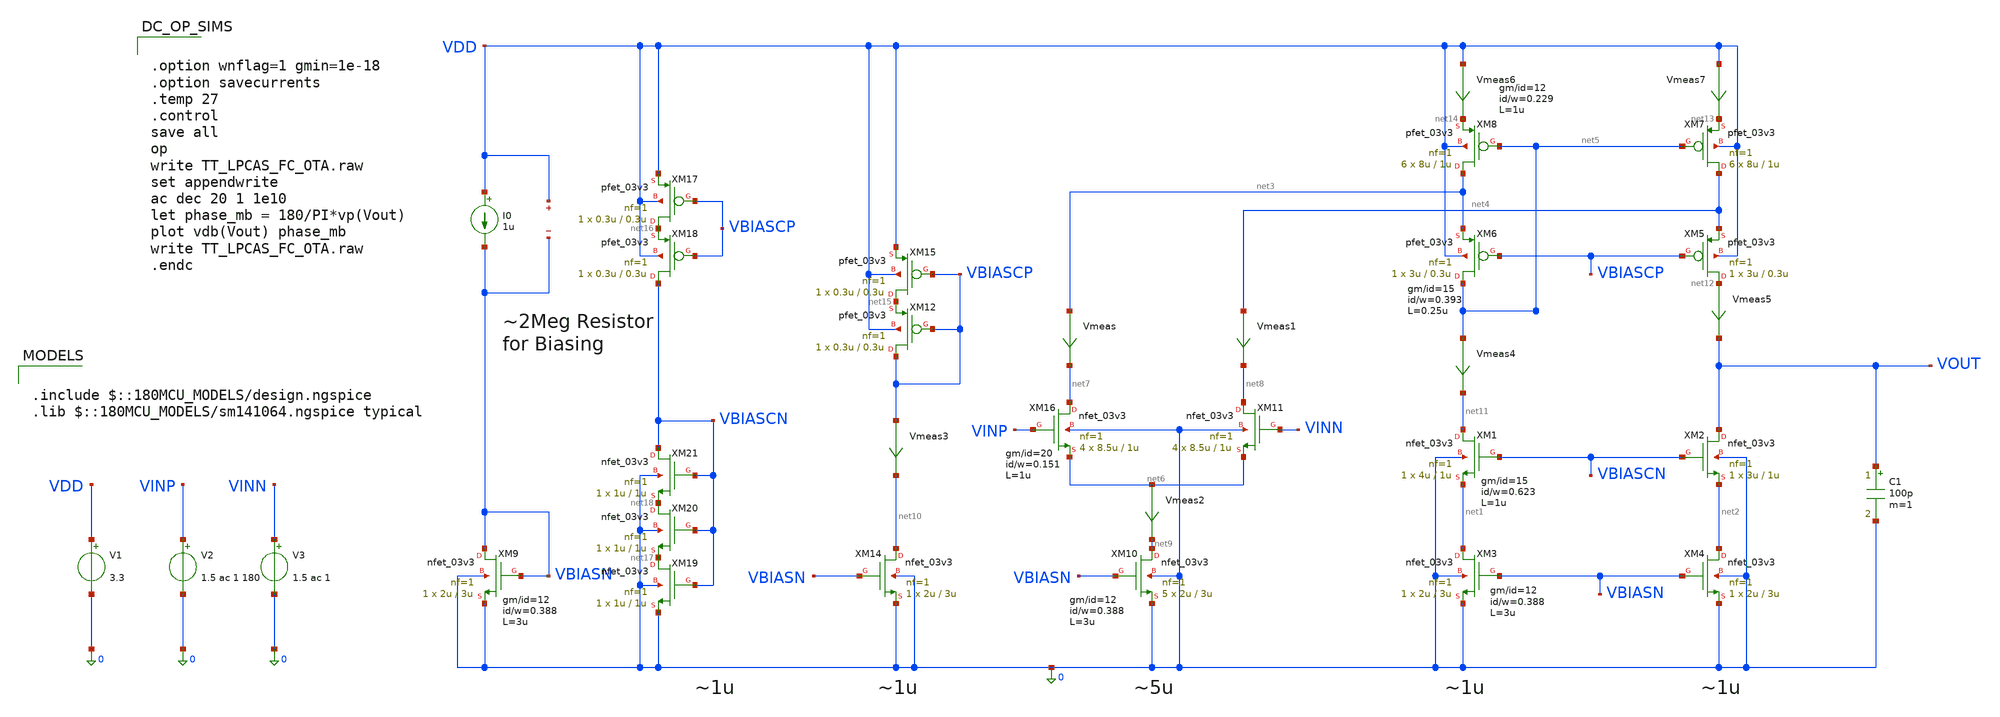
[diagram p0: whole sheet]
** sch_path: SCH/TT_LPCAS_FC_OTA.sch
**.subckt TT_LPCAS_FC_OTA
XM1 net11 VBIASCN net1 0 nfet_03v3 L=1u W=4u nf=1 ad='int((nf+1)/2) * W/nf * 0.18u' as='int((nf+2)/2) * W/nf * 0.18u'
+ pd='2*int((nf+1)/2) * (W/nf + 0.18u)' ps='2*int((nf+2)/2) * (W/nf + 0.18u)' nrd='0.18u / W' nrs='0.18u / W'
+ sa=0 sb=0 sd=0 m=1
XM2 VOUT VBIASCN net2 0 nfet_03v3 L=1u W=3u nf=1 ad='int((nf+1)/2) * W/nf * 0.18u' as='int((nf+2)/2) * W/nf * 0.18u'
+ pd='2*int((nf+1)/2) * (W/nf + 0.18u)' ps='2*int((nf+2)/2) * (W/nf + 0.18u)' nrd='0.18u / W' nrs='0.18u / W'
+ sa=0 sb=0 sd=0 m=1
XM5 net12 VBIASCP net4 VDD pfet_03v3 L=0.3u W=3u nf=1 ad='int((nf+1)/2) * W/nf * 0.18u' as='int((nf+2)/2) * W/nf * 0.18u'
+ pd='2*int((nf+1)/2) * (W/nf + 0.18u)' ps='2*int((nf+2)/2) * (W/nf + 0.18u)' nrd='0.18u / W' nrs='0.18u / W'
+ sa=0 sb=0 sd=0 m=1
XM6 net5 VBIASCP net3 VDD pfet_03v3 L=0.3u W=3u nf=1 ad='int((nf+1)/2) * W/nf * 0.18u' as='int((nf+2)/2) * W/nf * 0.18u'
+ pd='2*int((nf+1)/2) * (W/nf + 0.18u)' ps='2*int((nf+2)/2) * (W/nf + 0.18u)' nrd='0.18u / W' nrs='0.18u / W'
+ sa=0 sb=0 sd=0 m=1
XM7 net4 net5 net13 VDD pfet_03v3 L=1u W=8u nf=1 ad='int((nf+1)/2) * W/nf * 0.18u' as='int((nf+2)/2) * W/nf * 0.18u'
+ pd='2*int((nf+1)/2) * (W/nf + 0.18u)' ps='2*int((nf+2)/2) * (W/nf + 0.18u)' nrd='0.18u / W' nrs='0.18u / W'
+ sa=0 sb=0 sd=0 m=6
XM8 net3 net5 net14 VDD pfet_03v3 L=1u W=8u nf=1 ad='int((nf+1)/2) * W/nf * 0.18u' as='int((nf+2)/2) * W/nf * 0.18u'
+ pd='2*int((nf+1)/2) * (W/nf + 0.18u)' ps='2*int((nf+2)/2) * (W/nf + 0.18u)' nrd='0.18u / W' nrs='0.18u / W'
+ sa=0 sb=0 sd=0 m=6
XM9 VBIASN VBIASN 0 0 nfet_03v3 L=3u W=2u nf=1 ad='int((nf+1)/2) * W/nf * 0.18u' as='int((nf+2)/2) * W/nf * 0.18u'
+ pd='2*int((nf+1)/2) * (W/nf + 0.18u)' ps='2*int((nf+2)/2) * (W/nf + 0.18u)' nrd='0.18u / W' nrs='0.18u / W'
+ sa=0 sb=0 sd=0 m=1
XM10 net9 VBIASN 0 0 nfet_03v3 L=3u W=2u nf=1 ad='int((nf+1)/2) * W/nf * 0.18u' as='int((nf+2)/2) * W/nf * 0.18u'
+ pd='2*int((nf+1)/2) * (W/nf + 0.18u)' ps='2*int((nf+2)/2) * (W/nf + 0.18u)' nrd='0.18u / W' nrs='0.18u / W'
+ sa=0 sb=0 sd=0 m=5
XM3 net1 VBIASN 0 0 nfet_03v3 L=3u W=2u nf=1 ad='int((nf+1)/2) * W/nf * 0.18u' as='int((nf+2)/2) * W/nf * 0.18u'
+ pd='2*int((nf+1)/2) * (W/nf + 0.18u)' ps='2*int((nf+2)/2) * (W/nf + 0.18u)' nrd='0.18u / W' nrs='0.18u / W'
+ sa=0 sb=0 sd=0 m=1
XM4 net2 VBIASN 0 0 nfet_03v3 L=3u W=2u nf=1 ad='int((nf+1)/2) * W/nf * 0.18u' as='int((nf+2)/2) * W/nf * 0.18u'
+ pd='2*int((nf+1)/2) * (W/nf + 0.18u)' ps='2*int((nf+2)/2) * (W/nf + 0.18u)' nrd='0.18u / W' nrs='0.18u / W'
+ sa=0 sb=0 sd=0 m=1
XM14 net10 VBIASN 0 0 nfet_03v3 L=3u W=2u nf=1 ad='int((nf+1)/2) * W/nf * 0.18u' as='int((nf+2)/2) * W/nf * 0.18u'
+ pd='2*int((nf+1)/2) * (W/nf + 0.18u)' ps='2*int((nf+2)/2) * (W/nf + 0.18u)' nrd='0.18u / W' nrs='0.18u / W'
+ sa=0 sb=0 sd=0 m=1
XM15 net15 VBIASCP VDD VDD pfet_03v3 L=0.3u W=0.3u nf=1 ad='int((nf+1)/2) * W/nf * 0.18u' as='int((nf+2)/2) * W/nf * 0.18u'
+ pd='2*int((nf+1)/2) * (W/nf + 0.18u)' ps='2*int((nf+2)/2) * (W/nf + 0.18u)' nrd='0.18u / W' nrs='0.18u / W'
+ sa=0 sb=0 sd=0 m=1
I0 VDD VBIASN 1u
Vmeas net3 net7 0
.save i(vmeas)
Vmeas1 net4 net8 0
.save i(vmeas1)
Vmeas2 net6 net9 0
.save i(vmeas2)
Vmeas3 VBIASCP net10 0
.save i(vmeas3)
Vmeas4 net5 net11 0
.save i(vmeas4)
Vmeas5 net12 VOUT 0
.save i(vmeas5)
XM16 net7 VINP net6 0 nfet_03v3 L=1u W=8.5u nf=1 ad='int((nf+1)/2) * W/nf * 0.18u' as='int((nf+2)/2) * W/nf * 0.18u'
+ pd='2*int((nf+1)/2) * (W/nf + 0.18u)' ps='2*int((nf+2)/2) * (W/nf + 0.18u)' nrd='0.18u / W' nrs='0.18u / W'
+ sa=0 sb=0 sd=0 m=4
XM11 net8 VINN net6 0 nfet_03v3 L=1u W=8.5u nf=1 ad='int((nf+1)/2) * W/nf * 0.18u' as='int((nf+2)/2) * W/nf * 0.18u'
+ pd='2*int((nf+1)/2) * (W/nf + 0.18u)' ps='2*int((nf+2)/2) * (W/nf + 0.18u)' nrd='0.18u / W' nrs='0.18u / W'
+ sa=0 sb=0 sd=0 m=4
V1 VDD 0 3.3
V2 VINP 0 1.5 ac 1 180
V3 VINN 0 1.5 ac 1
Vmeas6 VDD net14 0
.save i(vmeas6)
Vmeas7 VDD net13 0
.save i(vmeas7)
C1 VOUT 0 100p m=1
XM12 VBIASCP VBIASCP net15 VDD pfet_03v3 L=0.3u W=0.3u nf=1 ad='int((nf+1)/2) * W/nf * 0.18u' as='int((nf+2)/2) * W/nf * 0.18u'
+ pd='2*int((nf+1)/2) * (W/nf + 0.18u)' ps='2*int((nf+2)/2) * (W/nf + 0.18u)' nrd='0.18u / W' nrs='0.18u / W'
+ sa=0 sb=0 sd=0 m=1
XM17 net16 VBIASCP VDD VDD pfet_03v3 L=0.3u W=0.3u nf=1 ad='int((nf+1)/2) * W/nf * 0.18u' as='int((nf+2)/2) * W/nf * 0.18u'
+ pd='2*int((nf+1)/2) * (W/nf + 0.18u)' ps='2*int((nf+2)/2) * (W/nf + 0.18u)' nrd='0.18u / W' nrs='0.18u / W'
+ sa=0 sb=0 sd=0 m=1
XM18 VBIASCN VBIASCP net16 VDD pfet_03v3 L=0.3u W=0.3u nf=1 ad='int((nf+1)/2) * W/nf * 0.18u' as='int((nf+2)/2) * W/nf * 0.18u'
+ pd='2*int((nf+1)/2) * (W/nf + 0.18u)' ps='2*int((nf+2)/2) * (W/nf + 0.18u)' nrd='0.18u / W' nrs='0.18u / W'
+ sa=0 sb=0 sd=0 m=1
XM19 net17 VBIASCN 0 0 nfet_03v3 L=1u W=1u nf=1 ad='int((nf+1)/2) * W/nf * 0.18u' as='int((nf+2)/2) * W/nf * 0.18u'
+ pd='2*int((nf+1)/2) * (W/nf + 0.18u)' ps='2*int((nf+2)/2) * (W/nf + 0.18u)' nrd='0.18u / W' nrs='0.18u / W'
+ sa=0 sb=0 sd=0 m=1
XM20 net18 VBIASCN net17 0 nfet_03v3 L=1u W=1u nf=1 ad='int((nf+1)/2) * W/nf * 0.18u' as='int((nf+2)/2) * W/nf * 0.18u'
+ pd='2*int((nf+1)/2) * (W/nf + 0.18u)' ps='2*int((nf+2)/2) * (W/nf + 0.18u)' nrd='0.18u / W' nrs='0.18u / W'
+ sa=0 sb=0 sd=0 m=1
XM21 VBIASCN VBIASCN net18 0 nfet_03v3 L=1u W=1u nf=1 ad='int((nf+1)/2) * W/nf * 0.18u' as='int((nf+2)/2) * W/nf * 0.18u'
+ pd='2*int((nf+1)/2) * (W/nf + 0.18u)' ps='2*int((nf+2)/2) * (W/nf + 0.18u)' nrd='0.18u / W' nrs='0.18u / W'
+ sa=0 sb=0 sd=0 m=1
.save v(vdd)
.save v(vbiasn)
**** begin user architecture code


.option wnflag=1 gmin=1e-18
.option savecurrents
.temp 27
.control
save all
op
write TT_LPCAS_FC_OTA.raw
set appendwrite
ac dec 20 1 1e10
let phase_mb = 180/PI*vp(Vout)
plot vdb(Vout) phase_mb
write TT_LPCAS_FC_OTA.raw
.endc



.include $::180MCU_MODELS/design.ngspice
.lib $::180MCU_MODELS/sm141064.ngspice typical

**** end user architecture code
**.ends
.end
